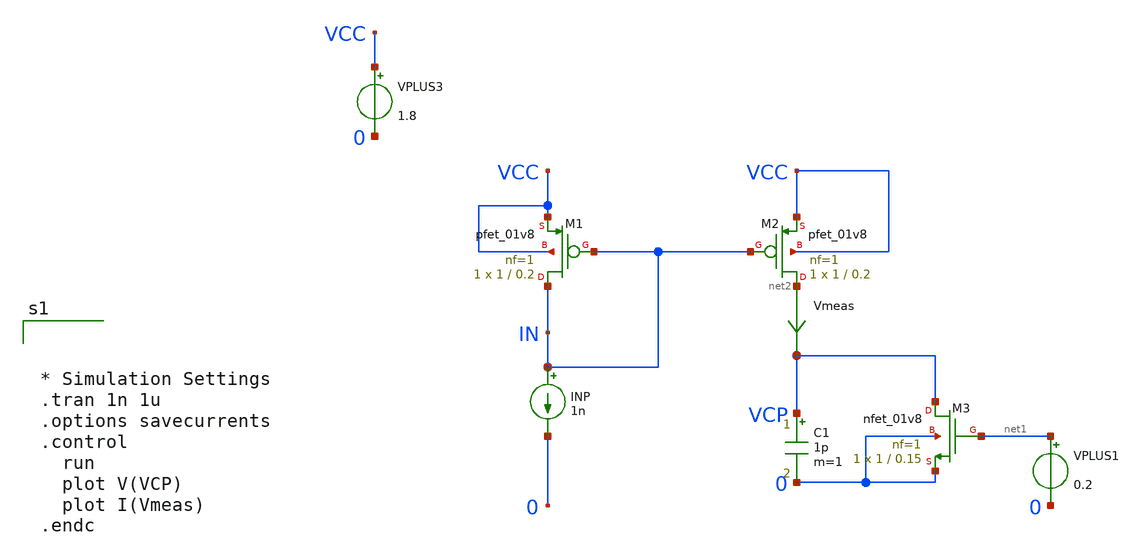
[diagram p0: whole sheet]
** sch_path: xschem/tb_cm.sch
**.subckt tb_cm
VPLUS3 VCC 0 1.8
INP IN 0 1n
XM1 IN IN VCC VCC sky130_fd_pr__pfet_01v8 L=0.2 W=1 nf=1 ad='int((nf+1)/2) * W/nf * 0.29' as='int((nf+2)/2) * W/nf * 0.29'
+ pd='2*int((nf+1)/2) * (W/nf + 0.29)' ps='2*int((nf+2)/2) * (W/nf + 0.29)' nrd='0.29 / W' nrs='0.29 / W'
+ sa=0 sb=0 sd=0 mult=1 m=1
XM2 net2 IN VCC VCC sky130_fd_pr__pfet_01v8 L=0.2 W=1 nf=1 ad='int((nf+1)/2) * W/nf * 0.29' as='int((nf+2)/2) * W/nf * 0.29'
+ pd='2*int((nf+1)/2) * (W/nf + 0.29)' ps='2*int((nf+2)/2) * (W/nf + 0.29)' nrd='0.29 / W' nrs='0.29 / W'
+ sa=0 sb=0 sd=0 mult=1 m=1
Vmeas net2 VCP 0
.save i(vmeas)
C1 VCP 0 1p m=1
XM3 VCP net1 0 0 sky130_fd_pr__nfet_01v8 L=0.15 W=1 nf=1 ad='int((nf+1)/2) * W/nf * 0.29' as='int((nf+2)/2) * W/nf * 0.29'
+ pd='2*int((nf+1)/2) * (W/nf + 0.29)' ps='2*int((nf+2)/2) * (W/nf + 0.29)' nrd='0.29 / W' nrs='0.29 / W'
+ sa=0 sb=0 sd=0 mult=1 m=1
VPLUS1 net1 0 0.2
**** begin user architecture code

** opencircuitdesign pdks install
.lib $::SKYWATER_MODELS/sky130.lib.spice tt





* Simulation Settings
.tran 1n 1u
.options savecurrents
.control
  run
  plot V(VCP)
  plot I(Vmeas)
.endc


**** end user architecture code
**.ends
.end
